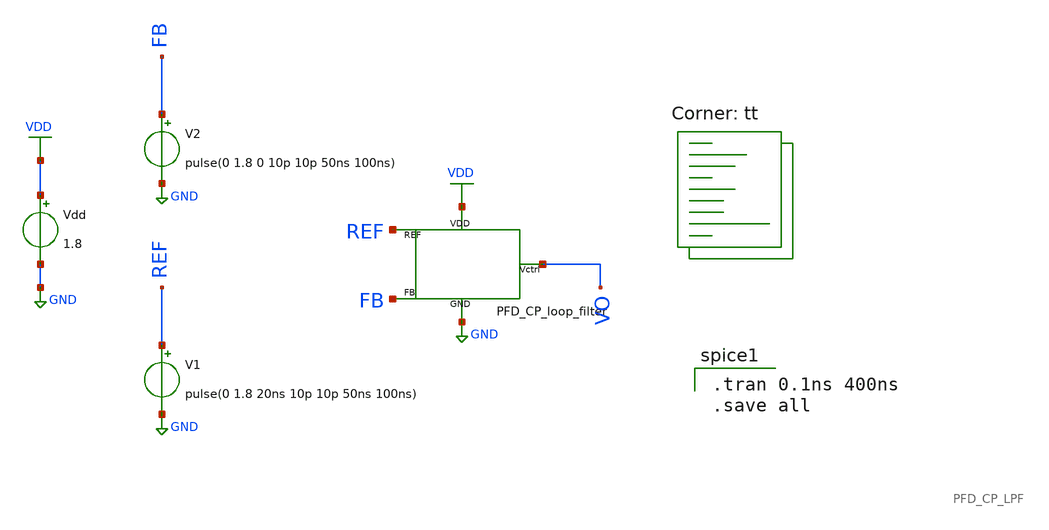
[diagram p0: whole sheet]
** sch_path: pll/pfd_cp_lf_lib/PFD_CP_LPF_tb/Xschem/PFD_CP_loop_filter.sch
**.subckt PFD_CP_loop_filter
Vdd VDD GND 1.8
PFD_CP_loop_filter REF FB VO VDD GND PFD_CP_LPF
V1 REF GND pulse(0 1.8 20ns 10p 10p 50ns 100ns)
V2 FB GND pulse(0 1.8 0 10p 10p 50ns 100ns)
**** begin user architecture code
.lib $::SKYWATER_MODELS/sky130.lib.spice tt

.tran 0.1ns 400ns
.save all

**** end user architecture code
**.ends
.GLOBAL GND
.GLOBAL VDD
.end
